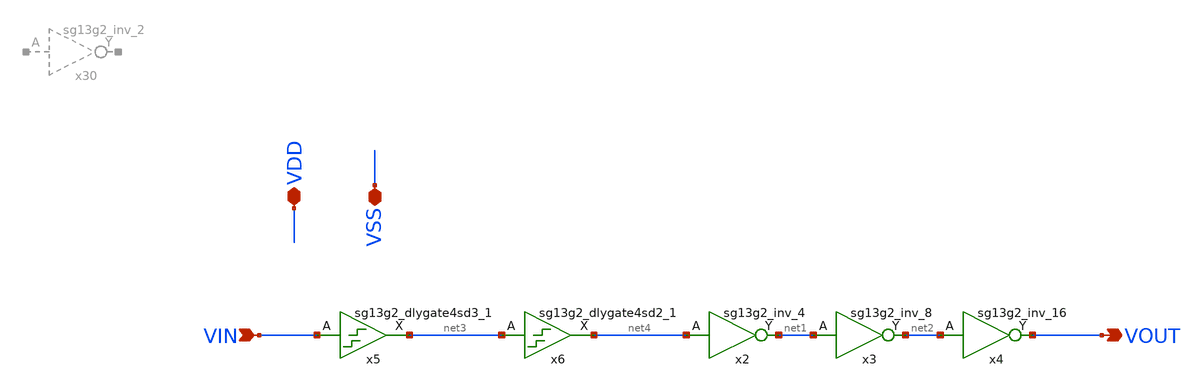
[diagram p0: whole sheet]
** sch_path: QDLL6501-main/schematic/xschem/DLine.sch
* IHP-GmbH/IHP-Open-PDK/ihp-sg13g2/libs.tech/xschem/sg13g2_stdcells/sg13g2_dlygate4sd2_1.sch:
* Copyright 2023 IHP PDK Authors
* Licensed under the Apache License, Version 2.0 (the "License");
**.subckt DLine VOUT VIN VDD VSS
*.opin VOUT
*.ipin VIN
*.iopin VDD
*.iopin VSS
x2 net1 net4 VDD VSS sg13g2_inv_4
x3 net2 net1 VDD VSS sg13g2_inv_8
x4 VOUT net2 VDD VSS sg13g2_inv_16
x5 net3 VIN VDD VSS sg13g2_dlygate4sd3_1
x6 net4 net3 VDD VSS sg13g2_dlygate4sd2_1
**.ends

* expanding   symbol:  sg13g2_stdcells/sg13g2_inv_2.sym # of pins=2
** sym_path: sg13g2_stdcells/sg13g2_inv_2.sym
** sch_path: sg13g2_stdcells/sg13g2_inv_2.sch
.subckt sg13g2_inv_2 Y A VDD VSS
*.opin Y
*.ipin A
*.iopin VDD
*.iopin VSS
XM1 Y A VSS VSS sg13_lv_nmos w=1.48u l=130.00n ng=2 m=1 mm_ok=1
XM2 Y A VDD VDD sg13_lv_pmos w=2.24u l=130.00n ng=2 m=1 mm_ok=1
.ends


* expanding   symbol:  sg13g2_stdcells/sg13g2_inv_4.sym # of pins=2
** sym_path: sg13g2_stdcells/sg13g2_inv_4.sym
** sch_path: sg13g2_stdcells/sg13g2_inv_4.sch
.subckt sg13g2_inv_4 Y A VDD VSS
*.ipin A
*.opin Y
*.iopin VDD
*.iopin VSS
XM1 Y A VSS VSS sg13_lv_nmos w=2.96u l=130.00n ng=4 m=1 mm_ok=1
XM2 Y A VDD VDD sg13_lv_pmos w=4.48u l=130.00n ng=4 m=1 mm_ok=1
.ends


* expanding   symbol:  sg13g2_stdcells/sg13g2_inv_8.sym # of pins=2
** sym_path: sg13g2_stdcells/sg13g2_inv_8.sym
** sch_path: sg13g2_stdcells/sg13g2_inv_8.sch
.subckt sg13g2_inv_8 Y A VDD VSS
*.opin Y
*.ipin A
*.iopin VDD
*.iopin VSS
XM1 Y A VSS VSS sg13_lv_nmos w=5.92u l=130.00n ng=8 m=1 mm_ok=1
XM2 Y A VDD VDD sg13_lv_pmos w=8.96u l=130.00n ng=8 m=1 mm_ok=1
.ends


* expanding   symbol:  sg13g2_stdcells/sg13g2_inv_16.sym # of pins=2
** sym_path: sg13g2_stdcells/sg13g2_inv_16.sym
** sch_path: sg13g2_stdcells/sg13g2_inv_16.sch
.subckt sg13g2_inv_16 Y A VDD VSS
*.opin Y
*.iopin VSS
*.ipin A
*.iopin VDD
XM1 Y A VSS VSS sg13_lv_nmos w=11.84u l=130.00n ng=16 m=1 mm_ok=1
XM2 Y A VDD VDD sg13_lv_pmos w=17.92u l=130.00n ng=16 m=1 mm_ok=1
.ends


* expanding   symbol:  sg13g2_stdcells/sg13g2_dlygate4sd3_1.sym # of pins=2
** sym_path: sg13g2_stdcells/sg13g2_dlygate4sd3_1.sym
** sch_path: sg13g2_stdcells/sg13g2_dlygate4sd3_1.sch
.subckt sg13g2_dlygate4sd3_1 X A VDD VSS
*.ipin A
*.opin X
*.iopin VDD
*.iopin VSS
XM1 net3 A VSS VSS sg13_lv_nmos w=420.00n l=130.00n ng=1 m=1 mm_ok=1
XM2 net1 net3 VSS VSS sg13_lv_nmos w=420.00n l=500.0n ng=1 m=1 mm_ok=1
XM3 net2 net1 VSS VSS sg13_lv_nmos w=420.00n l=500.0n ng=1 m=1 mm_ok=1
XM4 X net2 VSS VSS sg13_lv_nmos w=740.00n l=130.00n ng=1 m=1 mm_ok=1
XM5 net3 A VDD VDD sg13_lv_pmos w=420.00n l=130.00n ng=1 m=1 mm_ok=1
XM6 net1 net3 VDD VDD sg13_lv_pmos w=1.000u l=500.0n ng=1 m=1 mm_ok=1
XM7 net2 net1 VDD VDD sg13_lv_pmos w=1.000u l=500.0n ng=1 m=1 mm_ok=1
XM8 X net2 VDD VDD sg13_lv_pmos w=1.12u l=130.00n ng=1 m=1 mm_ok=1
.ends


* expanding   symbol:  sg13g2_stdcells/sg13g2_dlygate4sd2_1.sym # of pins=2
** sym_path: sg13g2_stdcells/sg13g2_dlygate4sd2_1.sym
** sch_path: sg13g2_stdcells/sg13g2_dlygate4sd2_1.sch
.subckt sg13g2_dlygate4sd2_1 X A VDD VSS
*.ipin A
*.opin X
*.iopin VDD
*.iopin VSS
XM1 net2 A VSS VSS sg13_lv_nmos w=420.00n l=130.00n ng=1 m=1 mm_ok=1
XM2 net1 net2 VSS VSS sg13_lv_nmos w=420.00n l=180.00n ng=1 m=1 mm_ok=1
XM3 net3 net1 VSS VSS sg13_lv_nmos w=420.00n l=180.00n ng=1 m=1 mm_ok=1
XM4 X net3 VSS VSS sg13_lv_nmos w=740.00n l=130.00n ng=1 m=1 mm_ok=1
XM5 net2 A VDD VDD sg13_lv_pmos w=420.00n l=130.00n ng=1 m=1 mm_ok=1
XM6 net1 net2 VDD VDD sg13_lv_pmos w=1.000u l=250.00n ng=1 m=1 mm_ok=1
XM7 net3 net1 VDD VDD sg13_lv_pmos w=1.000u l=250.00n ng=1 m=1 mm_ok=1
XM8 X net3 VDD VDD sg13_lv_pmos w=1.12u l=130.00n ng=1 m=1 mm_ok=1
.ends

.end
